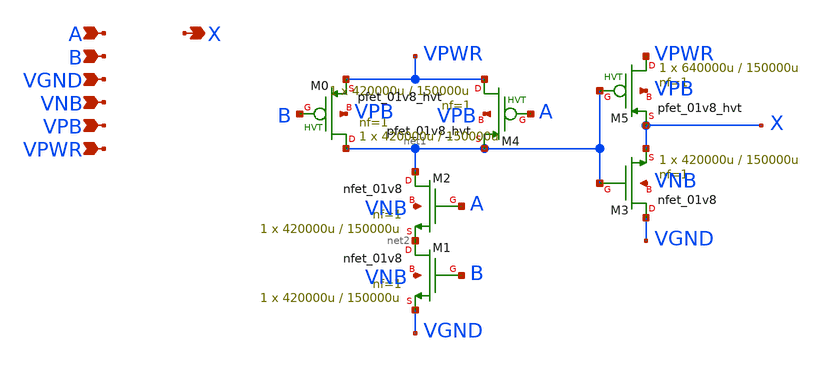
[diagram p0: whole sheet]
** sch_path: schematics/and2/sky130_fd_sc_hd__and2_0.sch
**.subckt sky130_fd_sc_hd__and2_0 A X B VGND VNB VPB VPWR
*.ipin A
*.opin X
*.ipin B
*.ipin VGND
*.ipin VNB
*.ipin VPB
*.ipin VPWR
XM4 VPWR A net1 VPB sky130_fd_pr__pfet_01v8_hvt L=150000u W=420000u nf=1 ad='int((1 + 1)/2) * 420000u / 1 * 0.29'
+ as='int((1 + 2)/2) * 420000u / 1 * 0.29' pd='2*int((1 + 1)/2) * (420000u / 1 + 0.29)' ps='2*int((1 + 2)/2) * (420000u / 1 + 0.29)'
+ nrd='0.29 / 420000u ' nrs='0.29 / 420000u ' sa=0 sb=0 sd=0 mult=1 m=1
XM0 net1 B VPWR VPB sky130_fd_pr__pfet_01v8_hvt L=150000u W=420000u nf=1 ad='int((1 + 1)/2) * 420000u / 1 * 0.29'
+ as='int((1 + 2)/2) * 420000u / 1 * 0.29' pd='2*int((1 + 1)/2) * (420000u / 1 + 0.29)' ps='2*int((1 + 2)/2) * (420000u / 1 + 0.29)'
+ nrd='0.29 / 420000u ' nrs='0.29 / 420000u ' sa=0 sb=0 sd=0 mult=1 m=1
XM2 net1 A net2 VNB sky130_fd_pr__nfet_01v8 L=150000u W=420000u nf=1 ad='int((1 + 1)/2) * 420000u / 1 * 0.29'
+ as='int((1 + 2)/2) * 420000u / 1 * 0.29' pd='2*int((1 + 1)/2) * (420000u / 1 + 0.29)' ps='2*int((1 + 2)/2) * (420000u / 1 + 0.29)'
+ nrd='0.29 / 420000u ' nrs='0.29 / 420000u ' sa=0 sb=0 sd=0 mult=1 m=1
XM1 net2 B VGND VNB sky130_fd_pr__nfet_01v8 L=150000u W=420000u nf=1 ad='int((1 + 1)/2) * 420000u / 1 * 0.29'
+ as='int((1 + 2)/2) * 420000u / 1 * 0.29' pd='2*int((1 + 1)/2) * (420000u / 1 + 0.29)' ps='2*int((1 + 2)/2) * (420000u / 1 + 0.29)'
+ nrd='0.29 / 420000u ' nrs='0.29 / 420000u ' sa=0 sb=0 sd=0 mult=1 m=1
XM3 VGND net1 X VNB sky130_fd_pr__nfet_01v8 L=150000u W=420000u nf=1 ad='int((1 + 1)/2) * 420000u / 1 * 0.29'
+ as='int((1 + 2)/2) * 420000u / 1 * 0.29' pd='2*int((1 + 1)/2) * (420000u / 1 + 0.29)' ps='2*int((1 + 2)/2) * (420000u / 1 + 0.29)'
+ nrd='0.29 / 420000u ' nrs='0.29 / 420000u ' sa=0 sb=0 sd=0 mult=1 m=1
XM5 VPWR net1 X VPB sky130_fd_pr__pfet_01v8_hvt L=150000u W=640000u nf=1 ad='int((1 + 1)/2) * 640000u / 1 * 0.29'
+ as='int((1 + 2)/2) * 640000u / 1 * 0.29' pd='2*int((1 + 1)/2) * (640000u / 1 + 0.29)' ps='2*int((1 + 2)/2) * (640000u / 1 + 0.29)'
+ nrd='0.29 / 640000u ' nrs='0.29 / 640000u ' sa=0 sb=0 sd=0 mult=1 m=1
**.ends
.end
